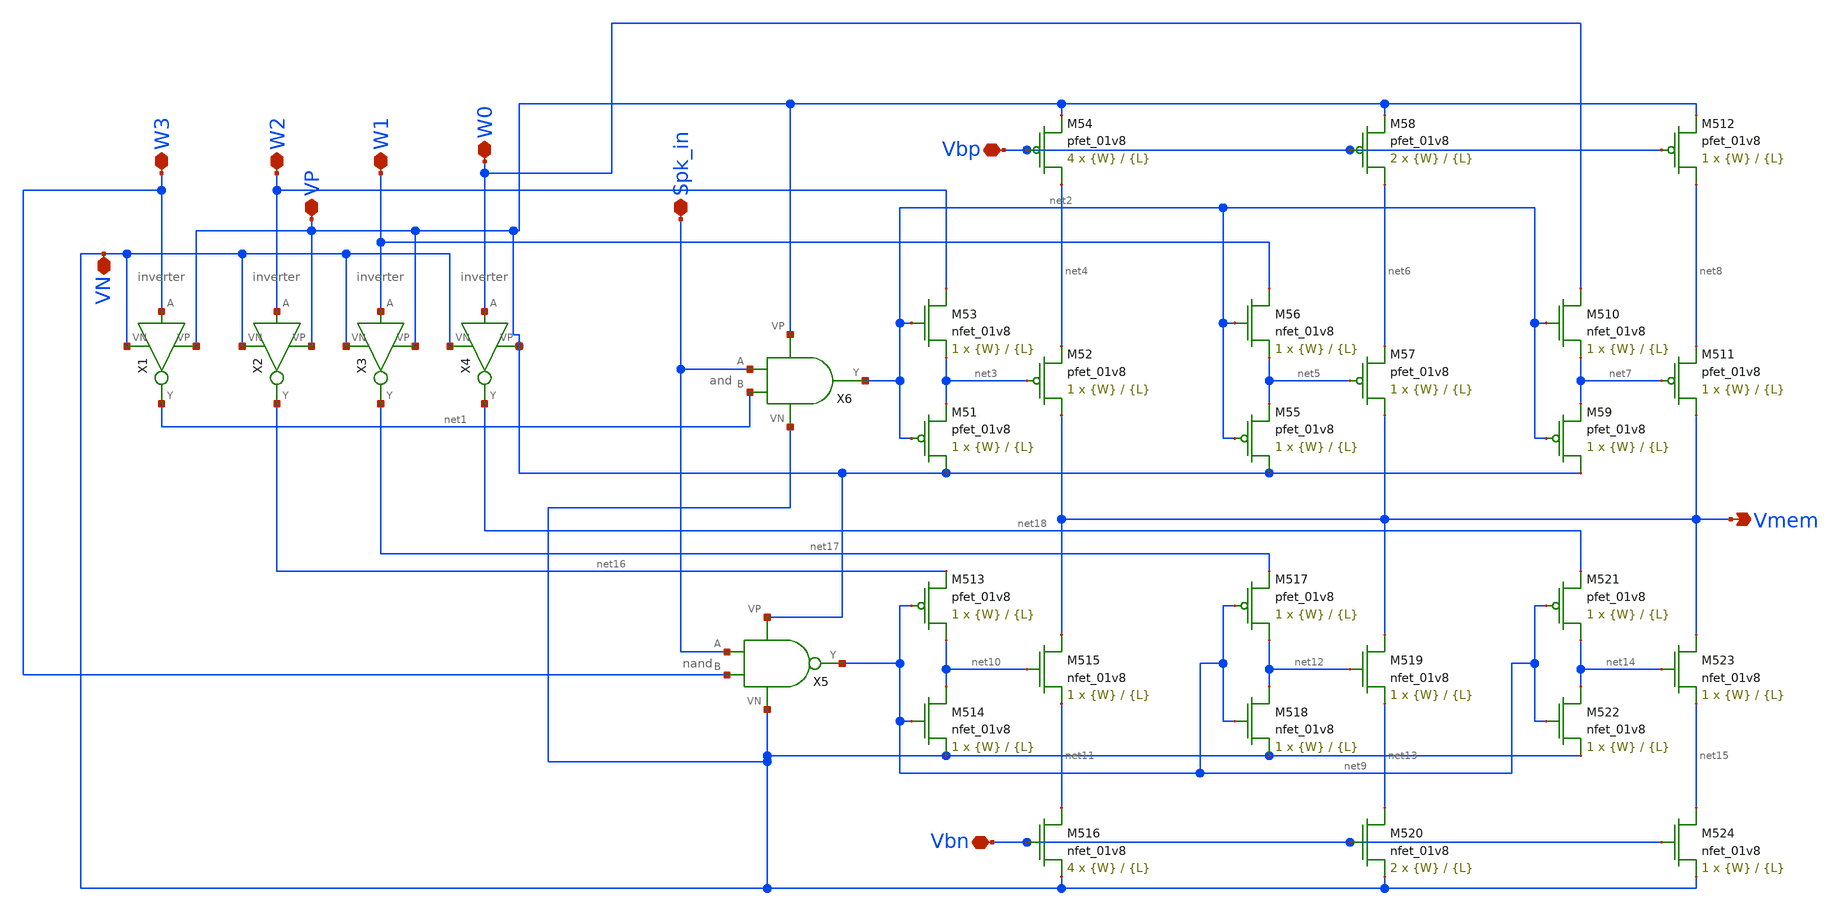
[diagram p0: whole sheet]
** sch_path: schematic/misc/BECI_asghar_synapse.sch
**.subckt BECI_asghar_synapse W3 W2 W1 W0 Vbp Vbn VP VN Spk_in Vmem
*.iopin W3
*.iopin W2
*.iopin W1
*.iopin W0
*.iopin Vbp
*.iopin Vbn
*.iopin VP
*.iopin VN
*.iopin Spk_in
*.opin Vmem
XM51 VP net2 net3 VDD sky130_fd_pr__pfet_01v8 L={L} W={W} nf=1 ad='int((nf+1)/2) * W/nf * 0.29' as='int((nf+2)/2) * W/nf * 0.29'
+ pd='2*int((nf+1)/2) * (W/nf + 0.29)' ps='2*int((nf+2)/2) * (W/nf + 0.29)' nrd='0.29 / W' nrs='0.29 / W'
+ sa=0 sb=0 sd=0 mult=1 m=1
XM53 W2 net2 net3 GND sky130_fd_pr__nfet_01v8 L={L} W={W} nf=1 ad='int((nf+1)/2) * W/nf * 0.29' as='int((nf+2)/2) * W/nf * 0.29'
+ pd='2*int((nf+1)/2) * (W/nf + 0.29)' ps='2*int((nf+2)/2) * (W/nf + 0.29)' nrd='0.29 / W' nrs='0.29 / W'
+ sa=0 sb=0 sd=0 mult=1 m=1
XM52 Vmem net3 net4 VDD sky130_fd_pr__pfet_01v8 L={L} W={W} nf=1 ad='int((nf+1)/2) * W/nf * 0.29' as='int((nf+2)/2) * W/nf * 0.29'
+ pd='2*int((nf+1)/2) * (W/nf + 0.29)' ps='2*int((nf+2)/2) * (W/nf + 0.29)' nrd='0.29 / W' nrs='0.29 / W'
+ sa=0 sb=0 sd=0 mult=1 m=1
XM54 net4 Vbp VP VDD sky130_fd_pr__pfet_01v8 L={L} W={W} nf=1 ad='int((nf+1)/2) * W/nf * 0.29' as='int((nf+2)/2) * W/nf * 0.29'
+ pd='2*int((nf+1)/2) * (W/nf + 0.29)' ps='2*int((nf+2)/2) * (W/nf + 0.29)' nrd='0.29 / W' nrs='0.29 / W'
+ sa=0 sb=0 sd=0 mult=4 m=4
XM55 VP net2 net5 VDD sky130_fd_pr__pfet_01v8 L={L} W={W} nf=1 ad='int((nf+1)/2) * W/nf * 0.29' as='int((nf+2)/2) * W/nf * 0.29'
+ pd='2*int((nf+1)/2) * (W/nf + 0.29)' ps='2*int((nf+2)/2) * (W/nf + 0.29)' nrd='0.29 / W' nrs='0.29 / W'
+ sa=0 sb=0 sd=0 mult=1 m=1
XM56 W1 net2 net5 GND sky130_fd_pr__nfet_01v8 L={L} W={W} nf=1 ad='int((nf+1)/2) * W/nf * 0.29' as='int((nf+2)/2) * W/nf * 0.29'
+ pd='2*int((nf+1)/2) * (W/nf + 0.29)' ps='2*int((nf+2)/2) * (W/nf + 0.29)' nrd='0.29 / W' nrs='0.29 / W'
+ sa=0 sb=0 sd=0 mult=1 m=1
XM57 Vmem net5 net6 VDD sky130_fd_pr__pfet_01v8 L={L} W={W} nf=1 ad='int((nf+1)/2) * W/nf * 0.29' as='int((nf+2)/2) * W/nf * 0.29'
+ pd='2*int((nf+1)/2) * (W/nf + 0.29)' ps='2*int((nf+2)/2) * (W/nf + 0.29)' nrd='0.29 / W' nrs='0.29 / W'
+ sa=0 sb=0 sd=0 mult=1 m=1
XM58 net6 Vbp VP VDD sky130_fd_pr__pfet_01v8 L={L} W={W} nf=1 ad='int((nf+1)/2) * W/nf * 0.29' as='int((nf+2)/2) * W/nf * 0.29'
+ pd='2*int((nf+1)/2) * (W/nf + 0.29)' ps='2*int((nf+2)/2) * (W/nf + 0.29)' nrd='0.29 / W' nrs='0.29 / W'
+ sa=0 sb=0 sd=0 mult=2 m=2
XM59 VP net2 net7 VDD sky130_fd_pr__pfet_01v8 L={L} W={W} nf=1 ad='int((nf+1)/2) * W/nf * 0.29' as='int((nf+2)/2) * W/nf * 0.29'
+ pd='2*int((nf+1)/2) * (W/nf + 0.29)' ps='2*int((nf+2)/2) * (W/nf + 0.29)' nrd='0.29 / W' nrs='0.29 / W'
+ sa=0 sb=0 sd=0 mult=1 m=1
XM510 W0 net2 net7 GND sky130_fd_pr__nfet_01v8 L={L} W={W} nf=1 ad='int((nf+1)/2) * W/nf * 0.29' as='int((nf+2)/2) * W/nf * 0.29'
+ pd='2*int((nf+1)/2) * (W/nf + 0.29)' ps='2*int((nf+2)/2) * (W/nf + 0.29)' nrd='0.29 / W' nrs='0.29 / W'
+ sa=0 sb=0 sd=0 mult=1 m=1
XM511 Vmem net7 net8 VDD sky130_fd_pr__pfet_01v8 L={L} W={W} nf=1 ad='int((nf+1)/2) * W/nf * 0.29' as='int((nf+2)/2) * W/nf * 0.29'
+ pd='2*int((nf+1)/2) * (W/nf + 0.29)' ps='2*int((nf+2)/2) * (W/nf + 0.29)' nrd='0.29 / W' nrs='0.29 / W'
+ sa=0 sb=0 sd=0 mult=1 m=1
XM512 net8 Vbp VP VDD sky130_fd_pr__pfet_01v8 L={L} W={W} nf=1 ad='int((nf+1)/2) * W/nf * 0.29' as='int((nf+2)/2) * W/nf * 0.29'
+ pd='2*int((nf+1)/2) * (W/nf + 0.29)' ps='2*int((nf+2)/2) * (W/nf + 0.29)' nrd='0.29 / W' nrs='0.29 / W'
+ sa=0 sb=0 sd=0 mult=1 m=1
XM513 net10 net9 net16 VDD sky130_fd_pr__pfet_01v8 L={L} W={W} nf=1 ad='int((nf+1)/2) * W/nf * 0.29'
+ as='int((nf+2)/2) * W/nf * 0.29' pd='2*int((nf+1)/2) * (W/nf + 0.29)' ps='2*int((nf+2)/2) * (W/nf + 0.29)'
+ nrd='0.29 / W' nrs='0.29 / W' sa=0 sb=0 sd=0 mult=1 m=1
XM514 net10 net9 VN GND sky130_fd_pr__nfet_01v8 L={L} W={W} nf=1 ad='int((nf+1)/2) * W/nf * 0.29' as='int((nf+2)/2) * W/nf * 0.29'
+ pd='2*int((nf+1)/2) * (W/nf + 0.29)' ps='2*int((nf+2)/2) * (W/nf + 0.29)' nrd='0.29 / W' nrs='0.29 / W'
+ sa=0 sb=0 sd=0 mult=1 m=1
XM515 Vmem net10 net11 GND sky130_fd_pr__nfet_01v8 L={L} W={W} nf=1 ad='int((nf+1)/2) * W/nf * 0.29'
+ as='int((nf+2)/2) * W/nf * 0.29' pd='2*int((nf+1)/2) * (W/nf + 0.29)' ps='2*int((nf+2)/2) * (W/nf + 0.29)'
+ nrd='0.29 / W' nrs='0.29 / W' sa=0 sb=0 sd=0 mult=1 m=1
XM516 net11 Vbn VN GND sky130_fd_pr__nfet_01v8 L={L} W={W} nf=1 ad='int((nf+1)/2) * W/nf * 0.29' as='int((nf+2)/2) * W/nf * 0.29'
+ pd='2*int((nf+1)/2) * (W/nf + 0.29)' ps='2*int((nf+2)/2) * (W/nf + 0.29)' nrd='0.29 / W' nrs='0.29 / W'
+ sa=0 sb=0 sd=0 mult=4 m=4
XM517 net12 net9 net17 VDD sky130_fd_pr__pfet_01v8 L={L} W={W} nf=1 ad='int((nf+1)/2) * W/nf * 0.29'
+ as='int((nf+2)/2) * W/nf * 0.29' pd='2*int((nf+1)/2) * (W/nf + 0.29)' ps='2*int((nf+2)/2) * (W/nf + 0.29)'
+ nrd='0.29 / W' nrs='0.29 / W' sa=0 sb=0 sd=0 mult=1 m=1
XM518 net12 net9 VN GND sky130_fd_pr__nfet_01v8 L={L} W={W} nf=1 ad='int((nf+1)/2) * W/nf * 0.29' as='int((nf+2)/2) * W/nf * 0.29'
+ pd='2*int((nf+1)/2) * (W/nf + 0.29)' ps='2*int((nf+2)/2) * (W/nf + 0.29)' nrd='0.29 / W' nrs='0.29 / W'
+ sa=0 sb=0 sd=0 mult=1 m=1
XM519 Vmem net12 net13 GND sky130_fd_pr__nfet_01v8 L={L} W={W} nf=1 ad='int((nf+1)/2) * W/nf * 0.29'
+ as='int((nf+2)/2) * W/nf * 0.29' pd='2*int((nf+1)/2) * (W/nf + 0.29)' ps='2*int((nf+2)/2) * (W/nf + 0.29)'
+ nrd='0.29 / W' nrs='0.29 / W' sa=0 sb=0 sd=0 mult=1 m=1
XM520 net13 Vbn VN GND sky130_fd_pr__nfet_01v8 L={L} W={W} nf=1 ad='int((nf+1)/2) * W/nf * 0.29' as='int((nf+2)/2) * W/nf * 0.29'
+ pd='2*int((nf+1)/2) * (W/nf + 0.29)' ps='2*int((nf+2)/2) * (W/nf + 0.29)' nrd='0.29 / W' nrs='0.29 / W'
+ sa=0 sb=0 sd=0 mult=2 m=2
XM521 net14 net9 net18 VDD sky130_fd_pr__pfet_01v8 L={L} W={W} nf=1 ad='int((nf+1)/2) * W/nf * 0.29'
+ as='int((nf+2)/2) * W/nf * 0.29' pd='2*int((nf+1)/2) * (W/nf + 0.29)' ps='2*int((nf+2)/2) * (W/nf + 0.29)'
+ nrd='0.29 / W' nrs='0.29 / W' sa=0 sb=0 sd=0 mult=1 m=1
XM522 net14 net9 VN GND sky130_fd_pr__nfet_01v8 L={L} W={W} nf=1 ad='int((nf+1)/2) * W/nf * 0.29' as='int((nf+2)/2) * W/nf * 0.29'
+ pd='2*int((nf+1)/2) * (W/nf + 0.29)' ps='2*int((nf+2)/2) * (W/nf + 0.29)' nrd='0.29 / W' nrs='0.29 / W'
+ sa=0 sb=0 sd=0 mult=1 m=1
XM523 Vmem net14 net15 GND sky130_fd_pr__nfet_01v8 L={L} W={W} nf=1 ad='int((nf+1)/2) * W/nf * 0.29'
+ as='int((nf+2)/2) * W/nf * 0.29' pd='2*int((nf+1)/2) * (W/nf + 0.29)' ps='2*int((nf+2)/2) * (W/nf + 0.29)'
+ nrd='0.29 / W' nrs='0.29 / W' sa=0 sb=0 sd=0 mult=1 m=1
XM524 net15 Vbn VN GND sky130_fd_pr__nfet_01v8 L={L} W={W} nf=1 ad='int((nf+1)/2) * W/nf * 0.29' as='int((nf+2)/2) * W/nf * 0.29'
+ pd='2*int((nf+1)/2) * (W/nf + 0.29)' ps='2*int((nf+2)/2) * (W/nf + 0.29)' nrd='0.29 / W' nrs='0.29 / W'
+ sa=0 sb=0 sd=0 mult=1 m=1
X6 Spk_in net1 net2 VP VN and
X5 Spk_in W3 net9 VP VN nand
X1 W3 VN VP net1 inverter
X2 W2 VN VP net16 inverter
X3 W1 VN VP net17 inverter
X4 W0 VN VP net18 inverter
**.ends
.end
